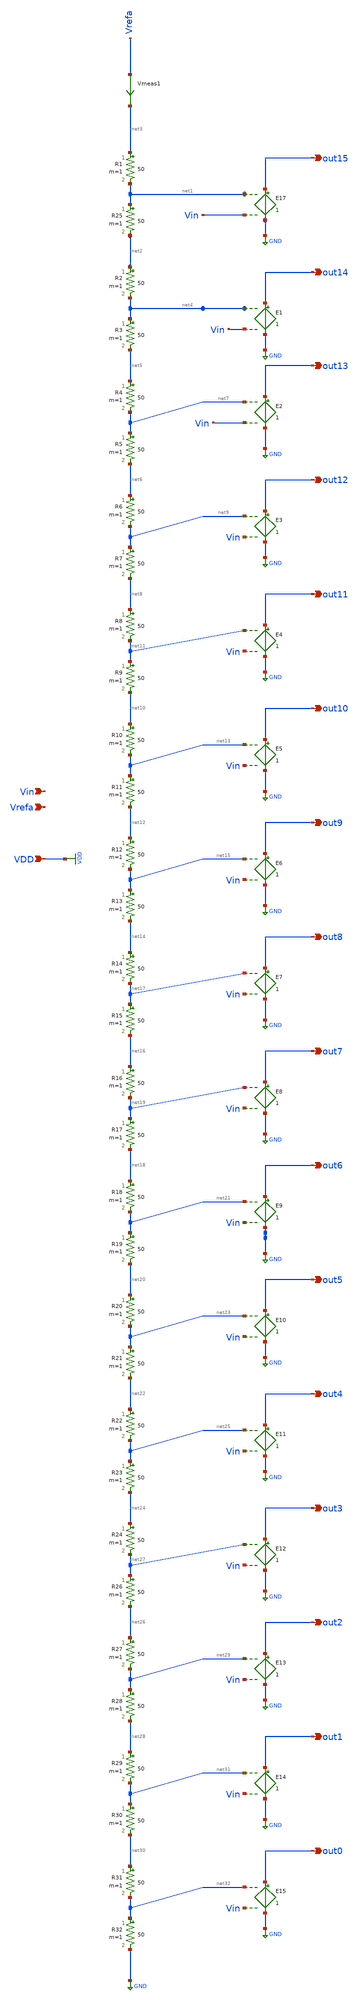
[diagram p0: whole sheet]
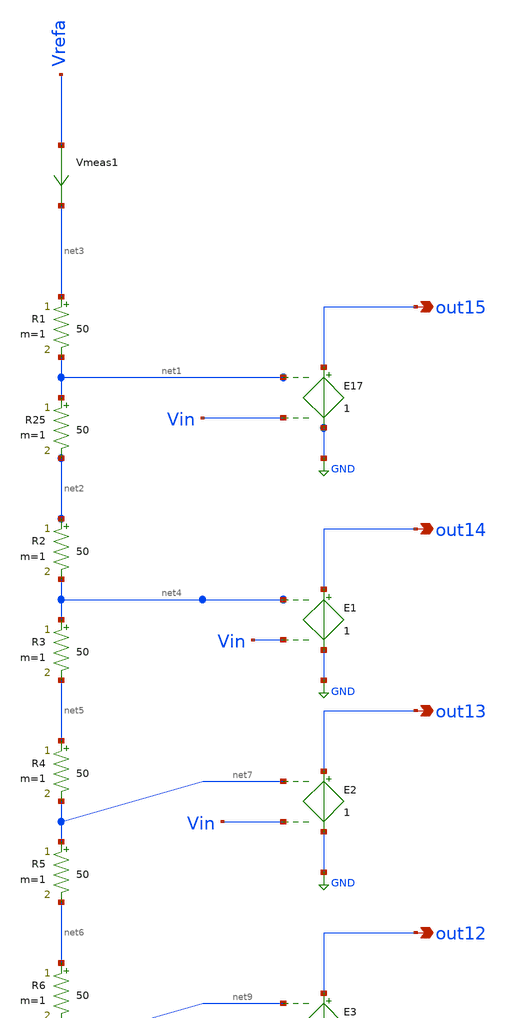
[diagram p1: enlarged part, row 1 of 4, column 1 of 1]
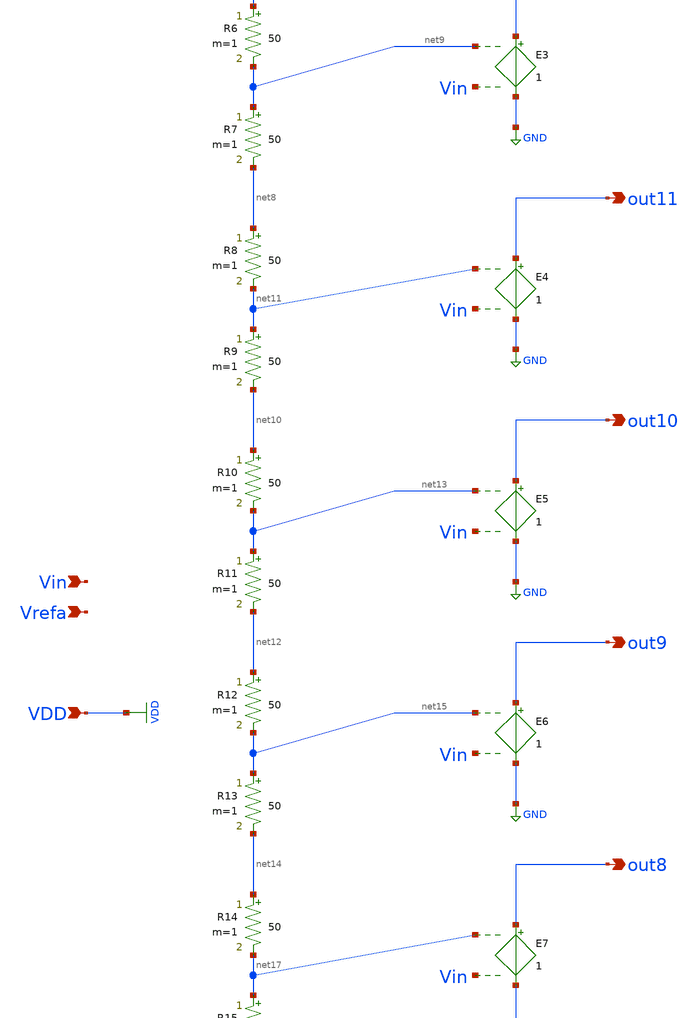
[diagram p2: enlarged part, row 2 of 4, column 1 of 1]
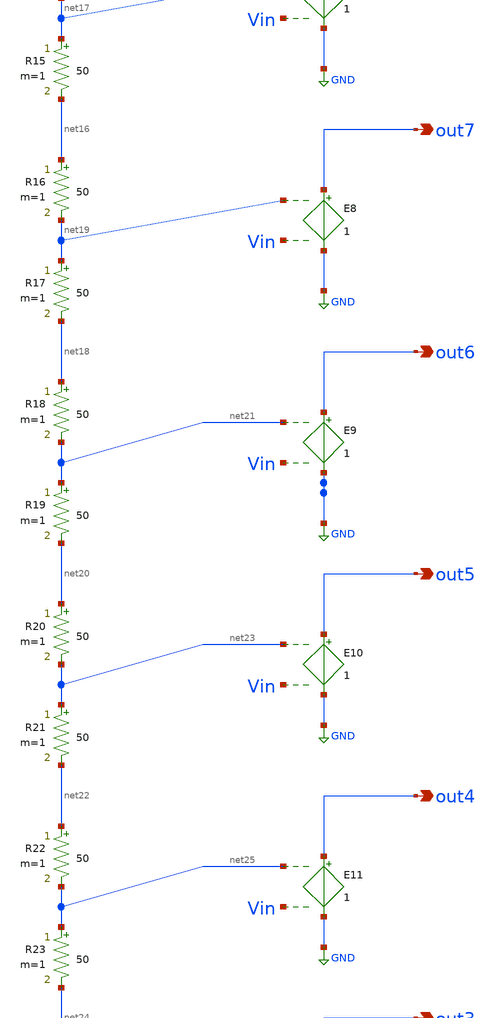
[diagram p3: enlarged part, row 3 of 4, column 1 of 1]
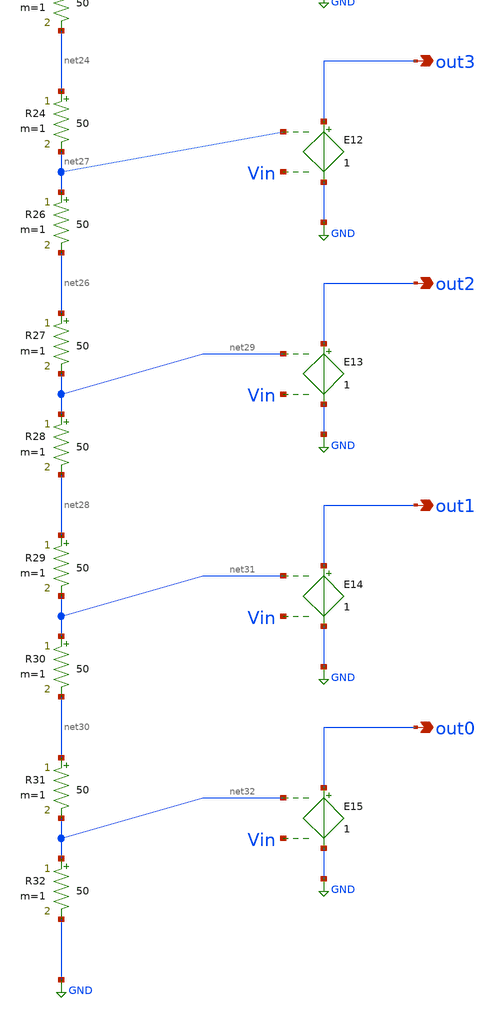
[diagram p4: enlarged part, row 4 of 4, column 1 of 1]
** sch_path: Ideal/IdealADC.sch
**.subckt IdealADC Vin Vrefa VDD out15 out14 out13 out12 out11 out10 out9 out8 out7 out6 out5 out4
*+ out3 out2 out1 out0
*.ipin Vin
*.ipin Vrefa
*.ipin VDD
*.opin out15
*.opin out14
*.opin out13
*.opin out12
*.opin out11
*.opin out10
*.opin out9
*.opin out8
*.opin out7
*.opin out6
*.opin out5
*.opin out4
*.opin out3
*.opin out2
*.opin out1
*.opin out0
Vmeas1 Vrefa net3 0
.save i(vmeas1)
R1 net3 net1 50 m=1
R25 net1 net2 50 m=1
E17 out15 GND net1 Vin 1
R2 net2 net4 50 m=1
R3 net4 net5 50 m=1
E1 out14 GND net4 Vin 1
R4 net5 net7 50 m=1
R5 net7 net6 50 m=1
E2 out13 GND net7 Vin 1
R6 net6 net9 50 m=1
R7 net9 net8 50 m=1
E3 out12 GND net9 Vin 1
R8 net8 net11 50 m=1
R9 net11 net10 50 m=1
E4 out11 GND net11 Vin 1
R10 net10 net13 50 m=1
R11 net13 net12 50 m=1
E5 out10 GND net13 Vin 1
R12 net12 net15 50 m=1
R13 net15 net14 50 m=1
E6 out9 GND net15 Vin 1
R14 net14 net17 50 m=1
R15 net17 net16 50 m=1
E7 out8 GND net17 Vin 1
R16 net16 net19 50 m=1
R17 net19 net18 50 m=1
E8 out7 GND net19 Vin 1
R18 net18 net21 50 m=1
R19 net21 net20 50 m=1
E9 out6 GND net21 Vin 1
R20 net20 net23 50 m=1
R21 net23 net22 50 m=1
E10 out5 GND net23 Vin 1
R22 net22 net25 50 m=1
R23 net25 net24 50 m=1
E11 out4 GND net25 Vin 1
R24 net24 net27 50 m=1
R26 net27 net26 50 m=1
E12 out3 GND net27 Vin 1
R27 net26 net29 50 m=1
R28 net29 net28 50 m=1
E13 out2 GND net29 Vin 1
R29 net28 net31 50 m=1
R30 net31 net30 50 m=1
E14 out1 GND net31 Vin 1
R31 net30 net32 50 m=1
R32 net32 GND 50 m=1
E15 out0 GND net32 Vin 1
**.ends
.GLOBAL VDD
.GLOBAL GND
.end
